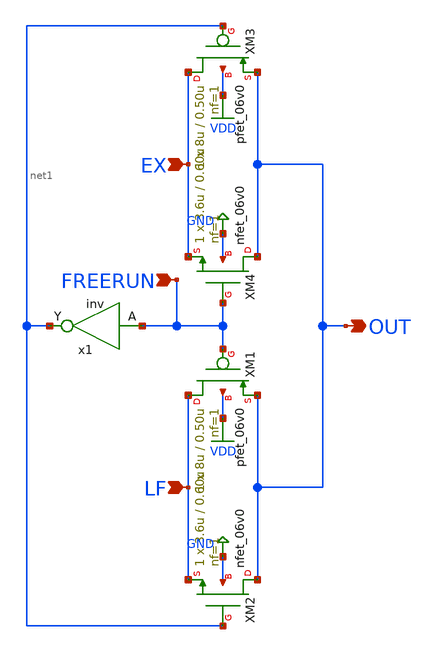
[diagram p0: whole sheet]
** sch_path: ctrlsel.sch
**.subckt ctrlsel OUT EX LF FREERUN
*.opin OUT
*.ipin EX
*.ipin LF
*.ipin FREERUN
XM1 LF FREERUN OUT VDD pfet_06v0 L=0.50u W=8u nf=1 ad='int((nf+1)/2) * W/nf * 0.18u' as='int((nf+2)/2) * W/nf * 0.18u'
+ pd='2*int((nf+1)/2) * (W/nf + 0.18u)' ps='2*int((nf+2)/2) * (W/nf + 0.18u)' nrd='0.18u / W' nrs='0.18u / W'
+ sa=0 sb=0 sd=0 m=1
XM2 OUT net1 LF GND nfet_06v0 L=0.60u W=3.6u nf=1 ad='int((nf+1)/2) * W/nf * 0.18u' as='int((nf+2)/2) * W/nf * 0.18u'
+ pd='2*int((nf+1)/2) * (W/nf + 0.18u)' ps='2*int((nf+2)/2) * (W/nf + 0.18u)' nrd='0.18u / W' nrs='0.18u / W'
+ sa=0 sb=0 sd=0 m=1
XM3 EX net1 OUT VDD pfet_06v0 L=0.50u W=8u nf=1 ad='int((nf+1)/2) * W/nf * 0.18u' as='int((nf+2)/2) * W/nf * 0.18u'
+ pd='2*int((nf+1)/2) * (W/nf + 0.18u)' ps='2*int((nf+2)/2) * (W/nf + 0.18u)' nrd='0.18u / W' nrs='0.18u / W'
+ sa=0 sb=0 sd=0 m=1
XM4 OUT FREERUN EX GND nfet_06v0 L=0.60u W=3.6u nf=1 ad='int((nf+1)/2) * W/nf * 0.18u' as='int((nf+2)/2) * W/nf * 0.18u'
+ pd='2*int((nf+1)/2) * (W/nf + 0.18u)' ps='2*int((nf+2)/2) * (W/nf + 0.18u)' nrd='0.18u / W' nrs='0.18u / W'
+ sa=0 sb=0 sd=0 m=1
x1 FREERUN net1 inv
**.ends

* expanding   symbol:  inv.sym # of pins=2
** sym_path: inv.sym
** sch_path: inv.sch
.subckt inv A Y
*.opin Y
*.ipin A
XM1 Y A VDD VDD pfet_06v0 L=0.50u W=2u nf=1 ad='int((nf+1)/2) * W/nf * 0.18u' as='int((nf+2)/2) * W/nf * 0.18u'
+ pd='2*int((nf+1)/2) * (W/nf + 0.18u)' ps='2*int((nf+2)/2) * (W/nf + 0.18u)' nrd='0.18u / W' nrs='0.18u / W'
+ sa=0 sb=0 sd=0 m=1
XM2 Y A GND GND nfet_06v0 L=0.60u W=0.9u nf=1 ad='int((nf+1)/2) * W/nf * 0.18u' as='int((nf+2)/2) * W/nf * 0.18u'
+ pd='2*int((nf+1)/2) * (W/nf + 0.18u)' ps='2*int((nf+2)/2) * (W/nf + 0.18u)' nrd='0.18u / W' nrs='0.18u / W'
+ sa=0 sb=0 sd=0 m=1
.ends

.GLOBAL GND
.GLOBAL VDD
.end
